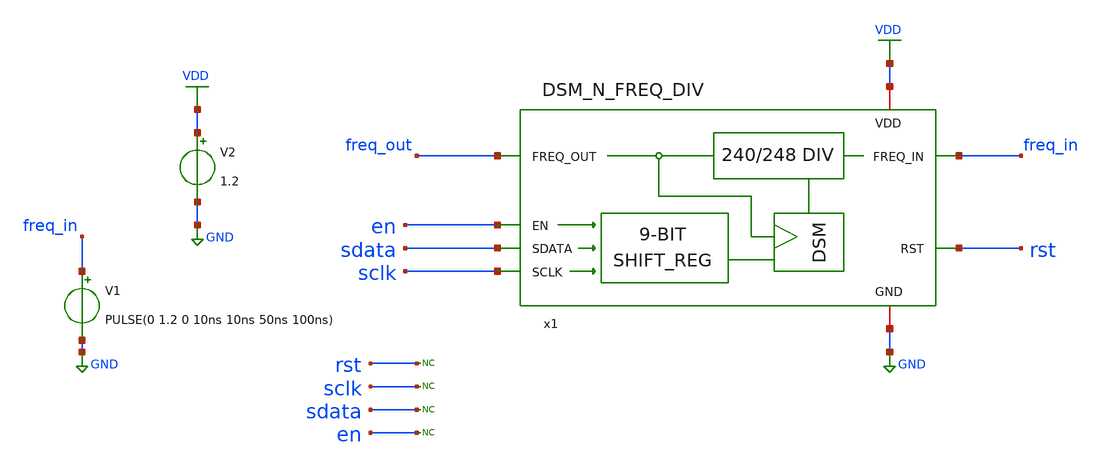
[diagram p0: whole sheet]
** sch_path: xschem/dsm/xschem/TEST.sch
* Copyright (C) 1998-2024 Stefan Frederik Schippers
* This program is free software; you can redistribute it and/or modify
* it under the terms of the GNU General Public License as published by
* the Free Software Foundation; either version 2 of the License, or
* (at your option) any later version.
* This program is distributed in the hope that it will be useful,
* but WITHOUT ANY WARRANTY; without even the implied warranty of
* MERCHANTABILITY or FITNESS FOR A PARTICULAR PURPOSE.  See the
* GNU General Public License for more details.
* You should have received a copy of the GNU General Public License
* along with this program; if not, write to the Free Software
**.subckt TEST
V1 freq_in GND PULSE(0 1.2 0 10ns 10ns 50ns 100ns)
* noconn rst
* noconn sclk
* noconn sdata
* noconn en
x1 [ freq_in rst sclk sdata en ] [ freq_out ] null dut
.model dut d_cosim simulation=../simulations/dsm_and_freq_divider.so
V2 VDD GND 1.2
**** begin user architecture code



.include ../DSM_N_FREQ_DIV.spice
* ngspice commands
.save v(dout) v(sdata) v(sclk) v(en) v(rst) v(dsm_clk) v(freq_in) v(freq_out)
.control
  tran 0.5n 1m
  remzerovec
  write test.raw
.endc

* to generate following file copy stimuli.test
* to the simulation directory and run simulation -> Utile Stimuli Editor (GUI),
* and press 'Translate'
.include stimuli_test.cir




.lib cornerMOSlv.lib mos_tt
.lib cornerMOShv.lib mos_tt
.lib cornerRES.lib res_typ
.lib cornerCAP.lib cap_typ

**** end user architecture code
**.ends
.GLOBAL GND
.GLOBAL VDD
.end
